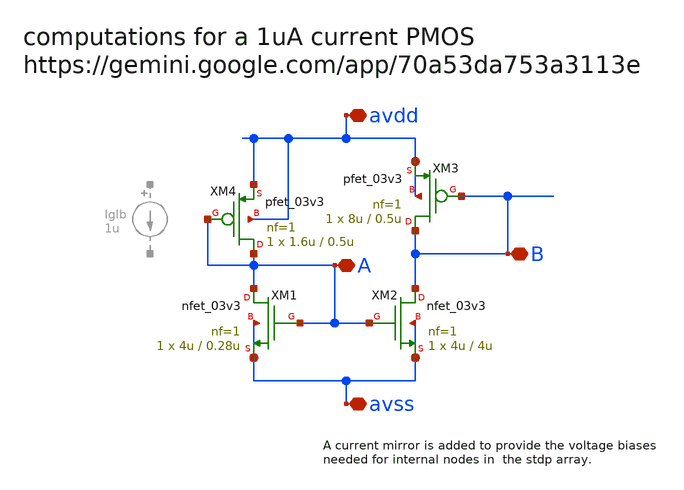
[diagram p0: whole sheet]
** sch_path: sch/untitled.sch
**.subckt untitled avdd avss B A
*.iopin avdd
*.iopin avss
*.iopin B
*.iopin A
XM1 A A avss avss nfet_03v3 L=0.28u W=4u nf=1 ad='int((nf+1)/2) * W/nf * 0.18u' as='int((nf+2)/2) * W/nf * 0.18u'
+ pd='2*int((nf+1)/2) * (W/nf + 0.18u)' ps='2*int((nf+2)/2) * (W/nf + 0.18u)' nrd='0.18u / W' nrs='0.18u / W'
+ sa=0 sb=0 sd=0 m=1
XM2 B A avss avss nfet_03v3 L=4u W=4u nf=1 ad='int((nf+1)/2) * W/nf * 0.18u' as='int((nf+2)/2) * W/nf * 0.18u'
+ pd='2*int((nf+1)/2) * (W/nf + 0.18u)' ps='2*int((nf+2)/2) * (W/nf + 0.18u)' nrd='0.18u / W' nrs='0.18u / W'
+ sa=0 sb=0 sd=0 m=1
XM3 B B avdd avdd pfet_03v3 L=0.5u W=8u nf=1 ad='int((nf+1)/2) * W/nf * 0.18u' as='int((nf+2)/2) * W/nf * 0.18u'
+ pd='2*int((nf+1)/2) * (W/nf + 0.18u)' ps='2*int((nf+2)/2) * (W/nf + 0.18u)' nrd='0.18u / W' nrs='0.18u / W'
+ sa=0 sb=0 sd=0 m=1
XM4 A A avdd avdd pfet_03v3 L=0.5u W=1.6u nf=1 ad='int((nf+1)/2) * W/nf * 0.18u' as='int((nf+2)/2) * W/nf * 0.18u'
+ pd='2*int((nf+1)/2) * (W/nf + 0.18u)' ps='2*int((nf+2)/2) * (W/nf + 0.18u)' nrd='0.18u / W' nrs='0.18u / W'
+ sa=0 sb=0 sd=0 m=1
**.ends
.end
